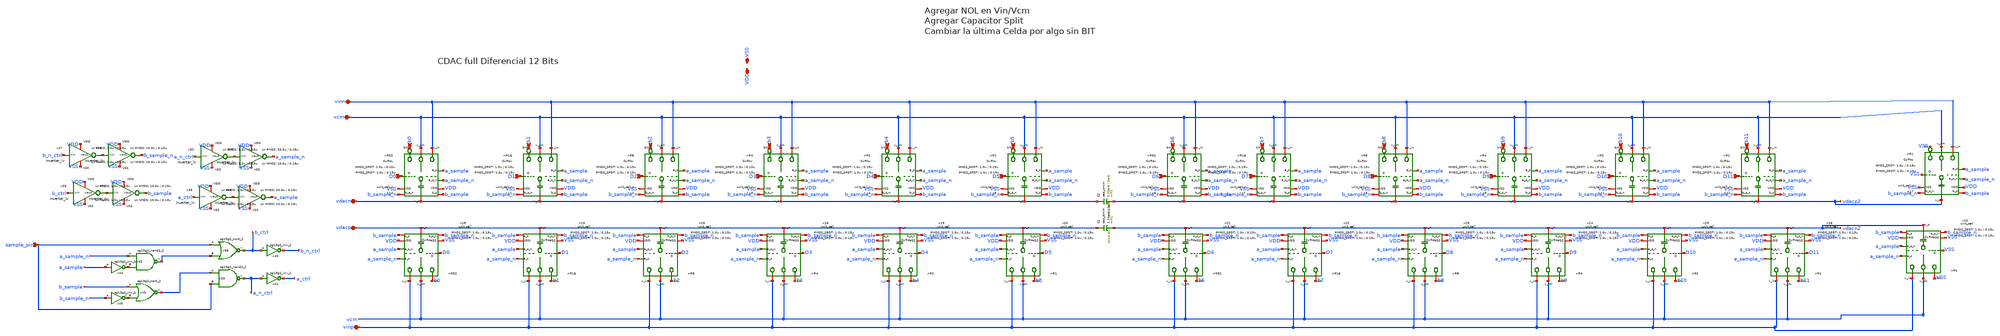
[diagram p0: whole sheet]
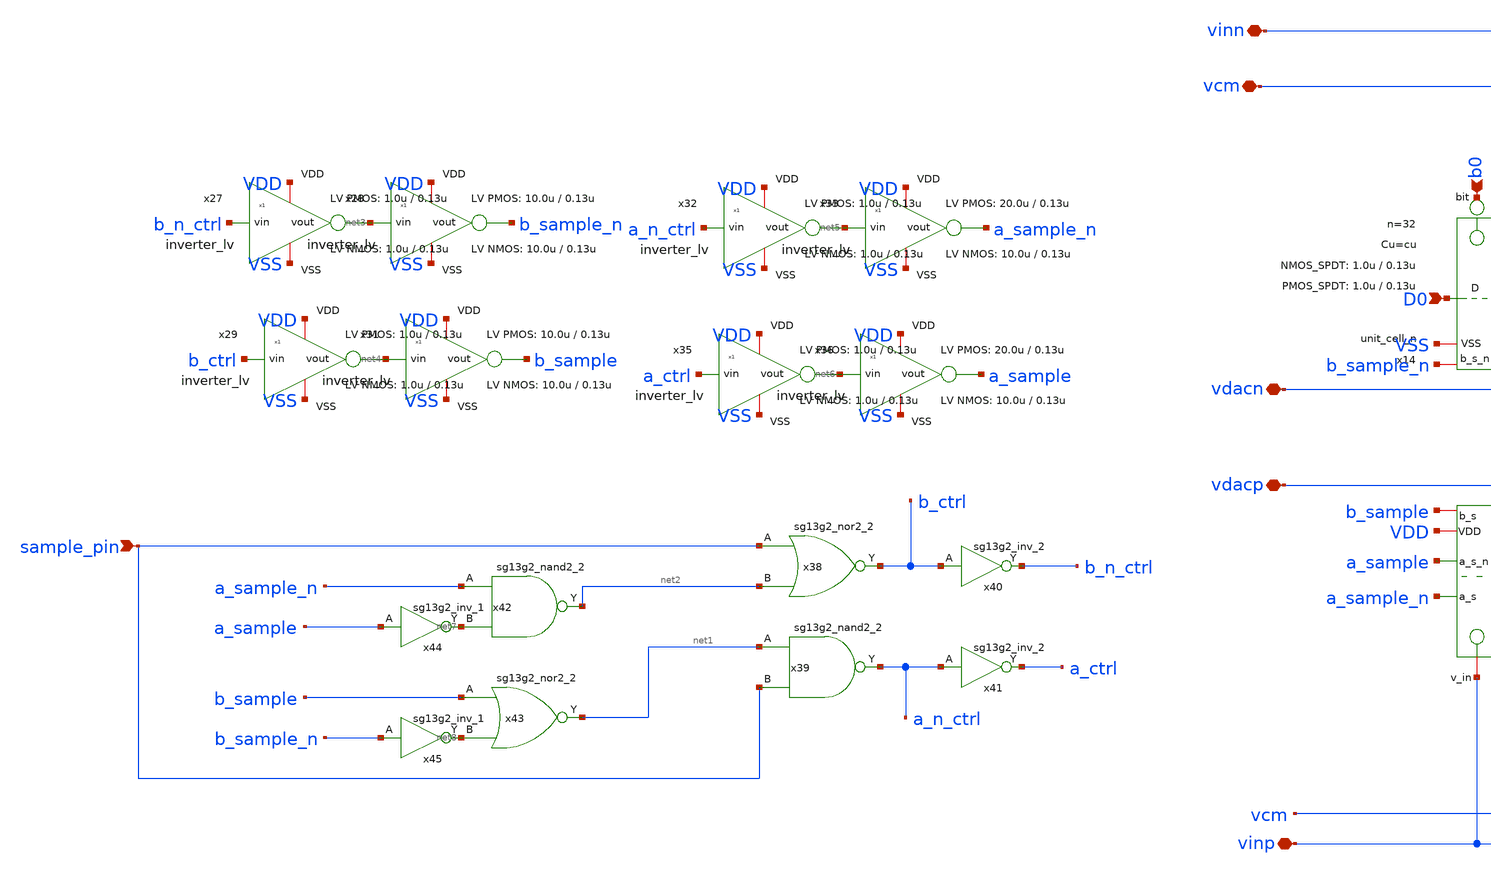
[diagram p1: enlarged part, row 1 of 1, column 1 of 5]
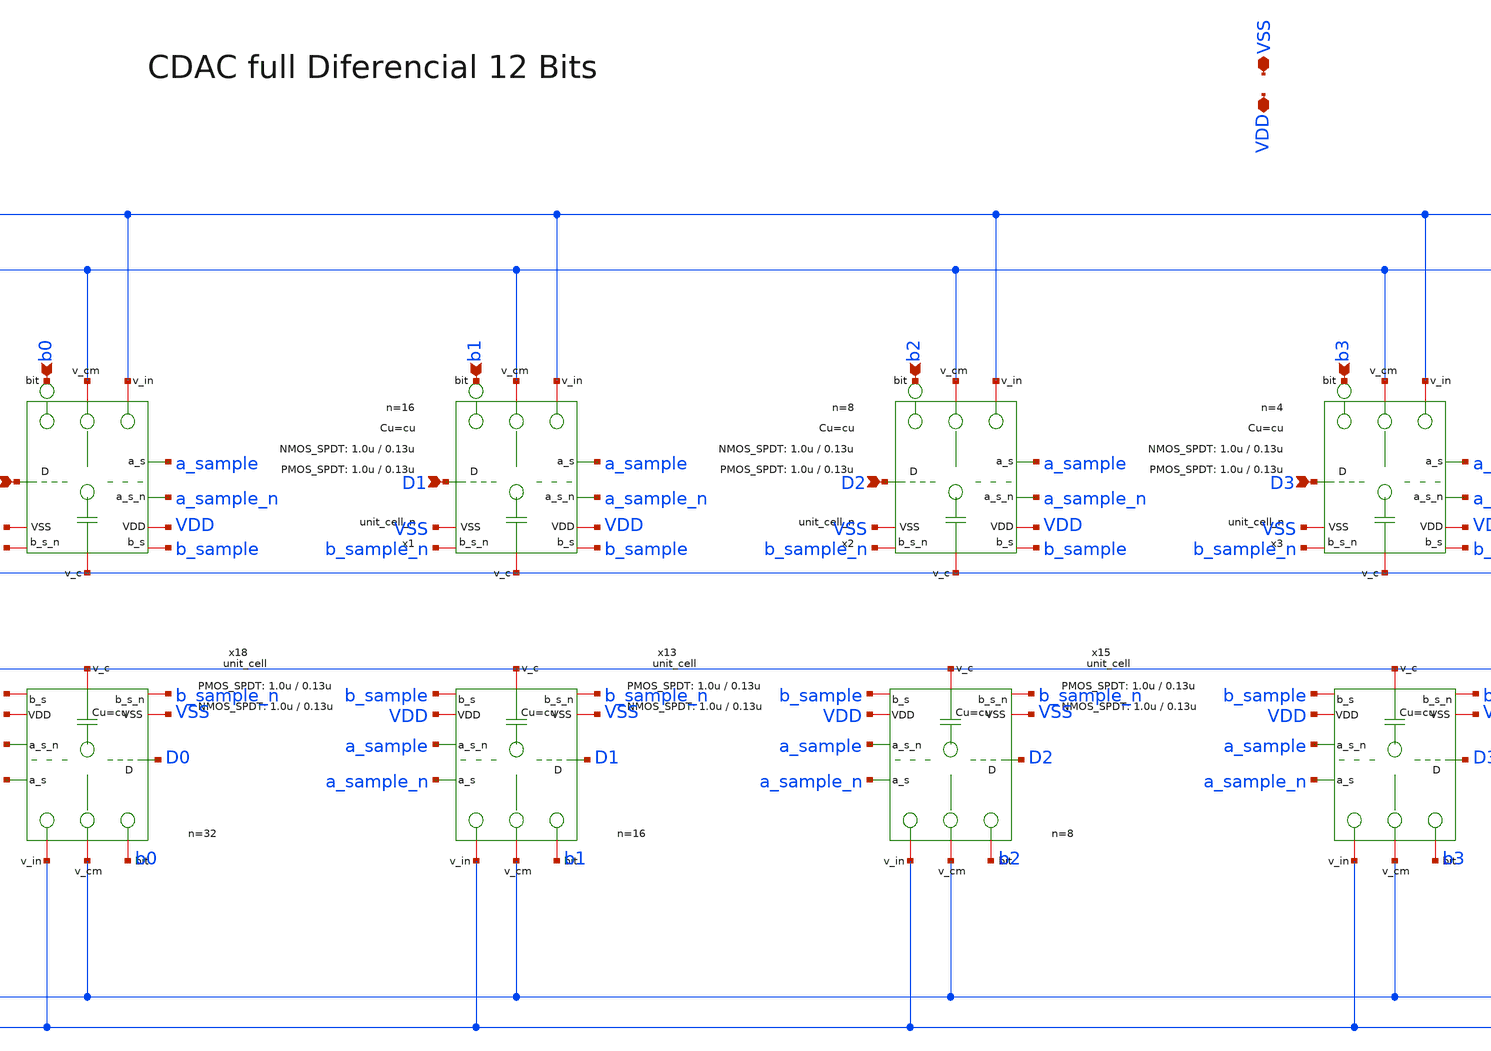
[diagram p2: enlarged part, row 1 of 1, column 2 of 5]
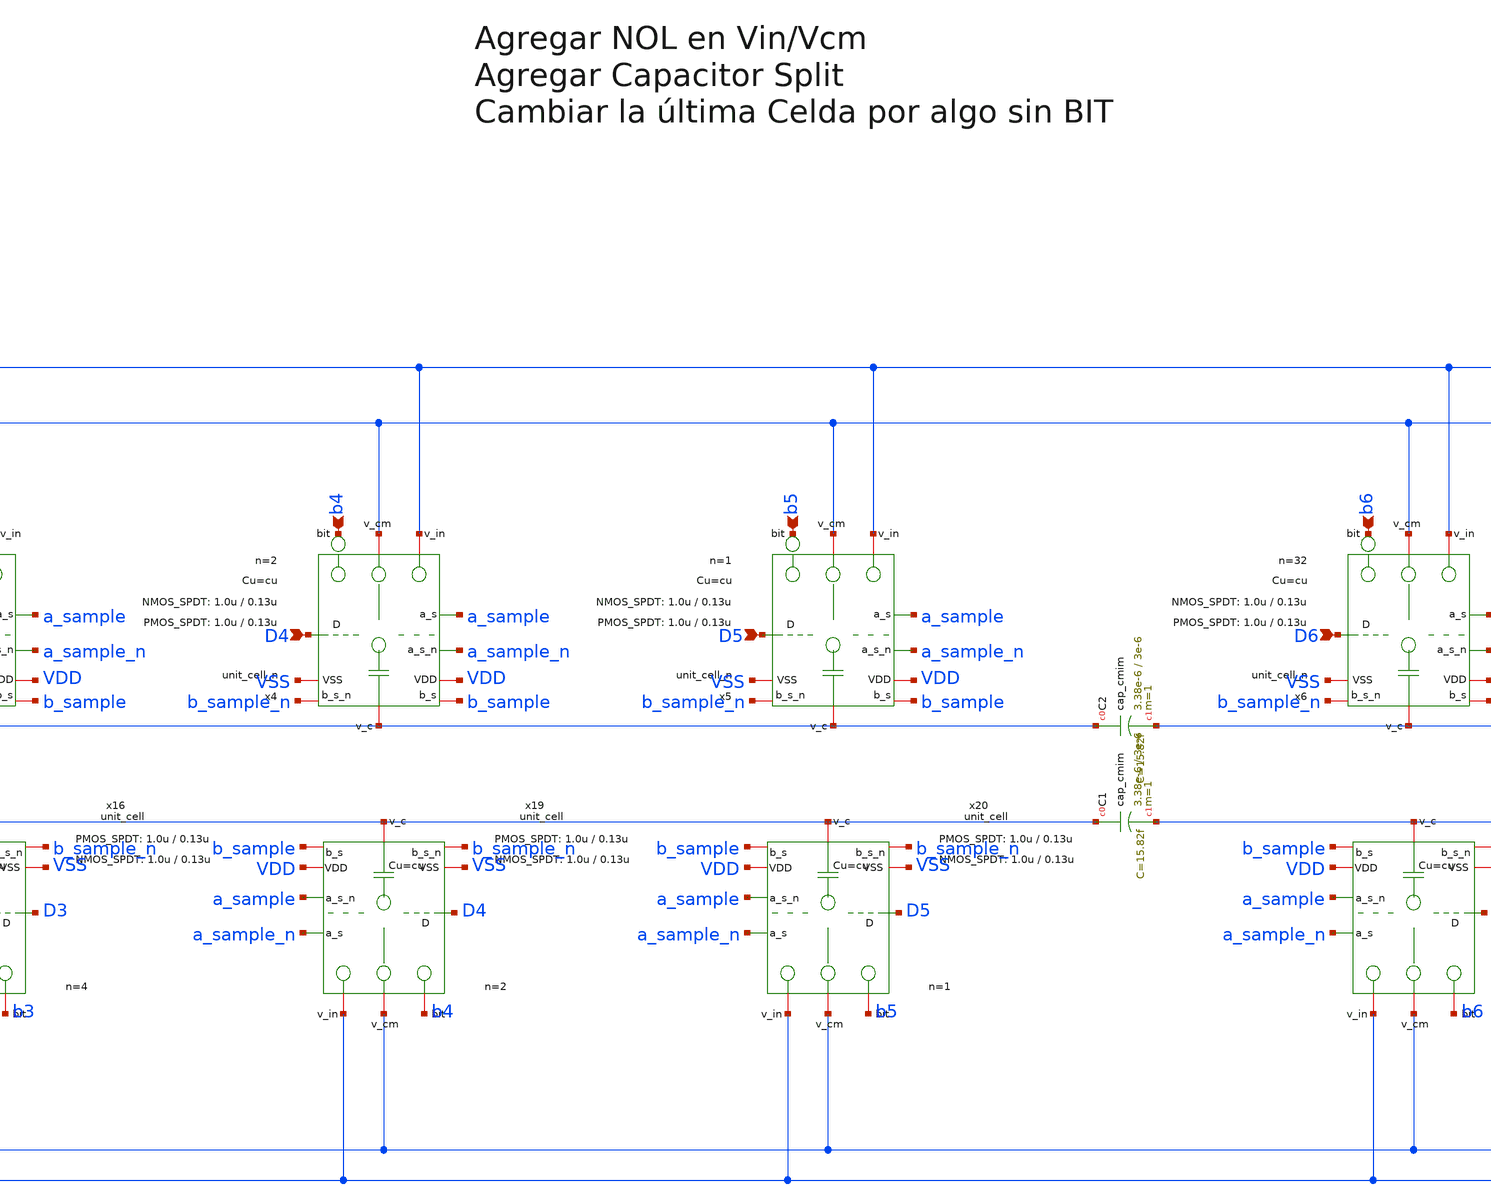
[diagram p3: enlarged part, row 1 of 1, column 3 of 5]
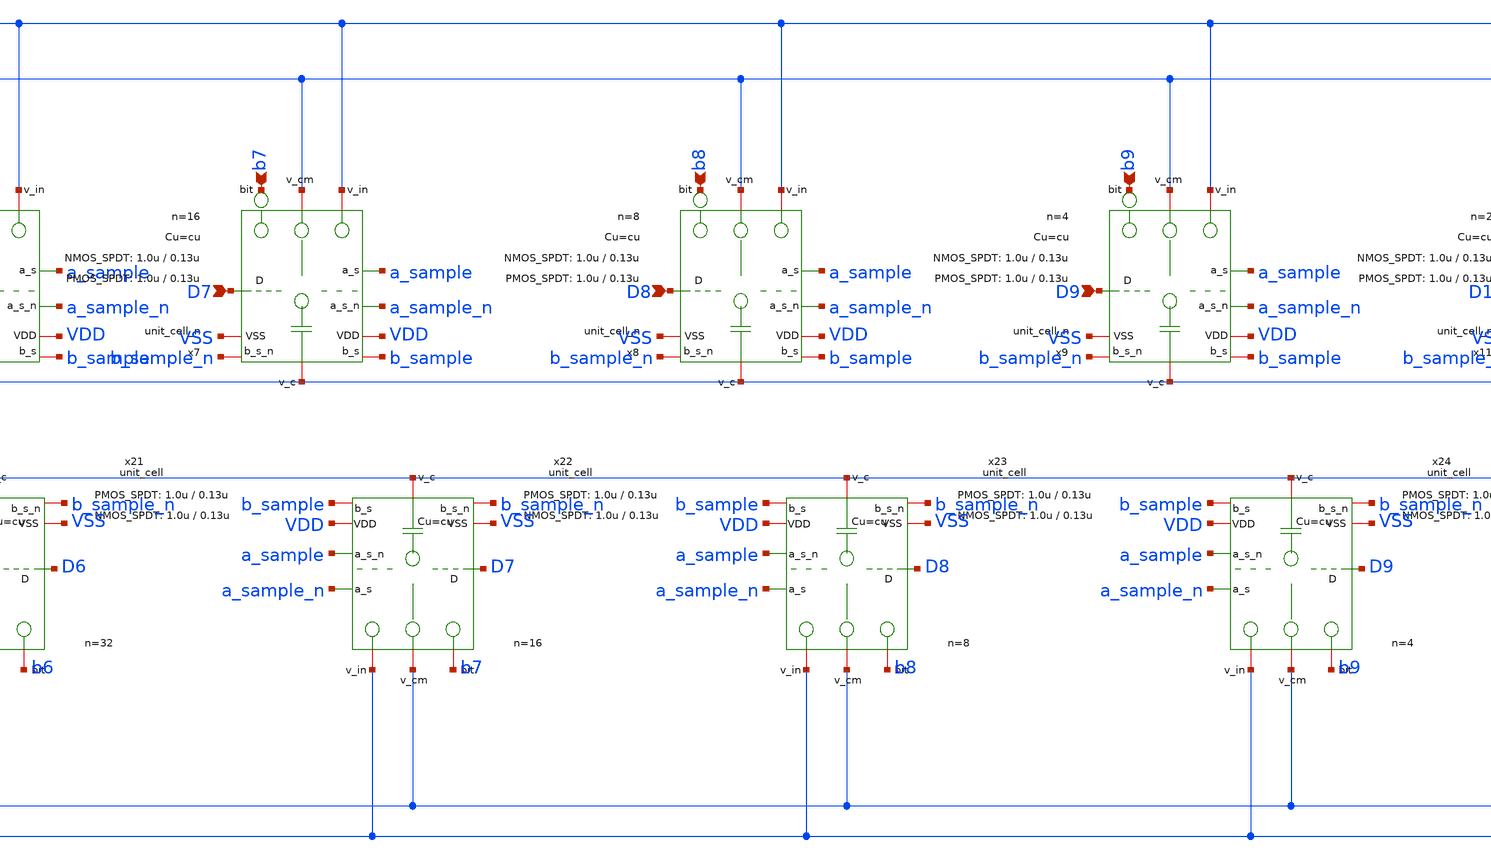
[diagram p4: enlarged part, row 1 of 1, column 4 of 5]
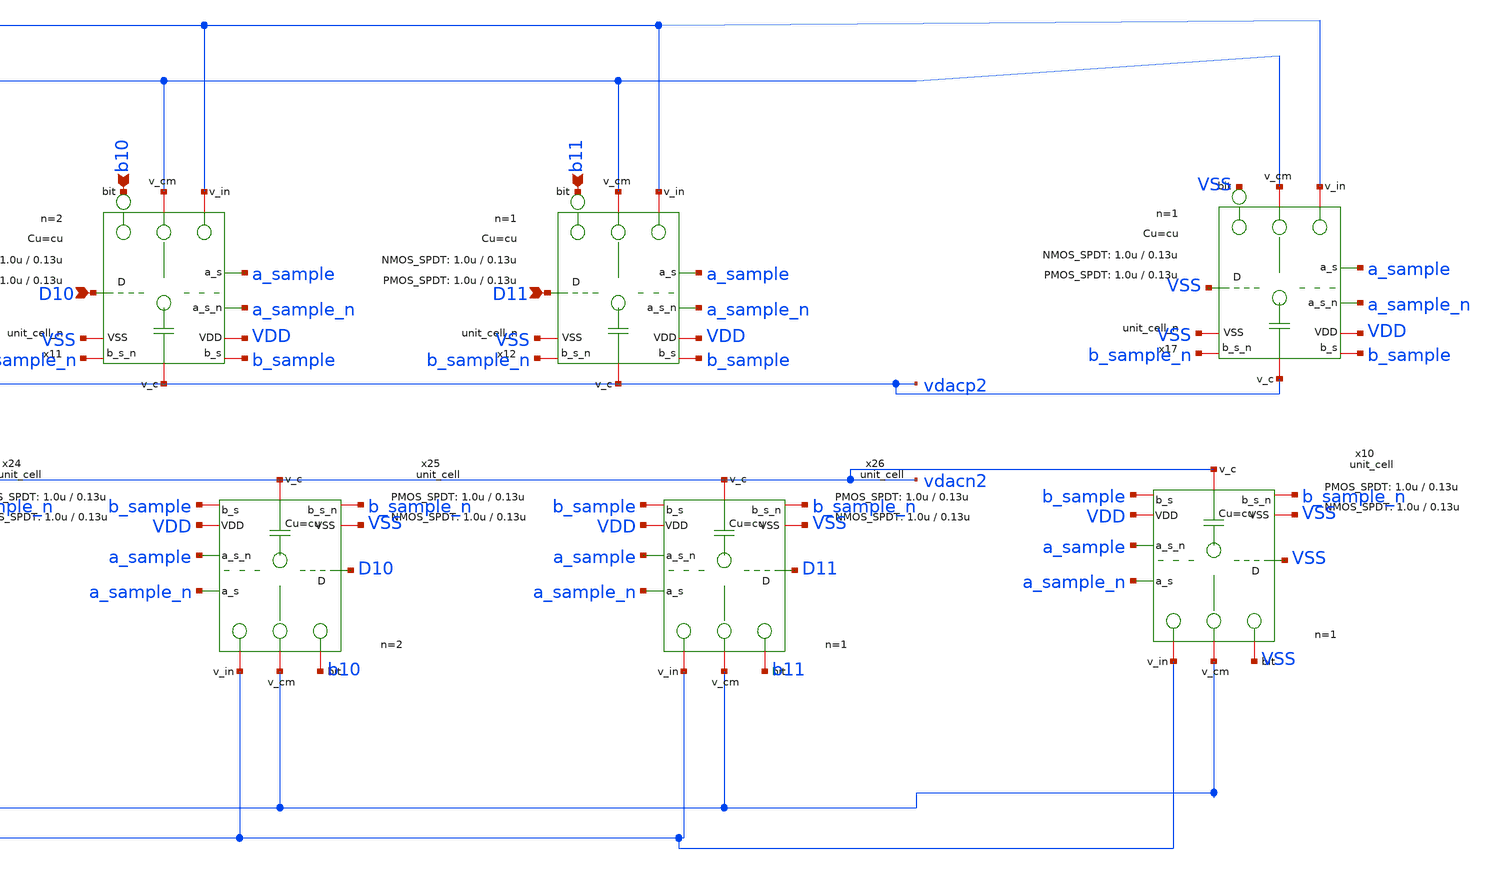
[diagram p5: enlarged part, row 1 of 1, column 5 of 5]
** sch_path: xschem/dac_icms_cell/dac.sch
* IHP-GmbH/IHP-Open-PDK/ihp-sg13g2/libs.tech/xschem/sg13g2_stdcells/sg13g2_inv_2.sch:
* Copyright 2023 IHP PDK Authors
* Licensed under the Apache License, Version 2.0 (the "License");
**.subckt dac D0 b0 vinp vcm sample_pin vinn vdacp vdacn VSS VDD D1 b1 D2 b2 D3 b3 D4 b4 D5 b5 D6 b6
*+ D7 b7 D8 b8 D9 b9 D10 b10 D11 b11
*.ipin D0
*.ipin b0
*.iopin vinp
*.iopin vcm
*.ipin sample_pin
*.iopin vinn
*.iopin vdacp
*.iopin vdacn
*.iopin VSS
*.iopin VDD
*.ipin D1
*.ipin b1
*.ipin D2
*.ipin b2
*.ipin D3
*.ipin b3
*.ipin D4
*.ipin b4
*.ipin D5
*.ipin b5
*.ipin D6
*.ipin b6
*.ipin D7
*.ipin b7
*.ipin D8
*.ipin b8
*.ipin D9
*.ipin b9
*.ipin D10
*.ipin b10
*.ipin D11
*.ipin b11
x14 VDD D0 VSS vdacn b0 vcm vinn a_sample a_sample_n b_sample b_sample_n unit_cell_n W_P=
+ L_P_SPDT=0.13u W_N= L_N_SPDT=0.13u Cu=cu n=32
x18 VDD D0 VSS vdacp b0 vcm vinp a_sample_n a_sample b_sample b_sample_n unit_cell W_P=
+ L_P_SPDT=0.13u W_N= L_N_SPDT=0.13u Cu=cu n=32
x1 VDD D1 VSS vdacn b1 vcm vinn a_sample a_sample_n b_sample b_sample_n unit_cell_n W_P=
+ L_P_SPDT=0.13u W_N= L_N_SPDT=0.13u Cu=cu n=16
x2 VDD D2 VSS vdacn b2 vcm vinn a_sample a_sample_n b_sample b_sample_n unit_cell_n W_P=
+ L_P_SPDT=0.13u W_N= L_N_SPDT=0.13u Cu=cu n=8
x3 VDD D3 VSS vdacn b3 vcm vinn a_sample a_sample_n b_sample b_sample_n unit_cell_n W_P=
+ L_P_SPDT=0.13u W_N= L_N_SPDT=0.13u Cu=cu n=4
x4 VDD D4 VSS vdacn b4 vcm vinn a_sample a_sample_n b_sample b_sample_n unit_cell_n W_P=1.0u
+ L_P_SPDT=0.13u W_N=1.0u L_N_SPDT=0.13u Cu=cu n=2
x5 VDD D5 VSS vdacn b5 vcm vinn a_sample a_sample_n b_sample b_sample_n unit_cell_n W_P=
+ L_P_SPDT=0.13u W_N= L_N_SPDT=0.13u Cu=cu n=1
x6 VDD D6 VSS vdacp2 b6 vcm vinn a_sample a_sample_n b_sample b_sample_n unit_cell_n W_P=
+ L_P_SPDT=0.13u W_N= L_N_SPDT=0.13u Cu=cu n=32
x7 VDD D7 VSS vdacp2 b7 vcm vinn a_sample a_sample_n b_sample b_sample_n unit_cell_n W_P=
+ L_P_SPDT=0.13u W_N= L_N_SPDT=0.13u Cu=cu n=16
x8 VDD D8 VSS vdacp2 b8 vcm vinn a_sample a_sample_n b_sample b_sample_n unit_cell_n W_P=
+ L_P_SPDT=0.13u W_N= L_N_SPDT=0.13u Cu=cu n=8
x9 VDD D9 VSS vdacp2 b9 vcm vinn a_sample a_sample_n b_sample b_sample_n unit_cell_n W_P=
+ L_P_SPDT=0.13u W_N= L_N_SPDT=0.13u Cu=cu n=4
x11 VDD D10 VSS vdacp2 b10 vcm vinn a_sample a_sample_n b_sample b_sample_n unit_cell_n W_P=
+ L_P_SPDT=0.13u W_N= L_N_SPDT=0.13u Cu=cu n=2
x12 VDD D11 VSS vdacp2 b11 vcm vinn a_sample a_sample_n b_sample b_sample_n unit_cell_n W_P=
+ L_P_SPDT=0.13u W_N= L_N_SPDT=0.13u Cu=cu n=1
x13 VDD D1 VSS vdacp b1 vcm vinp a_sample_n a_sample b_sample b_sample_n unit_cell W_P=
+ L_P_SPDT=0.13u W_N= L_N_SPDT=0.13u Cu=cu n=16
x15 VDD D2 VSS vdacp b2 vcm vinp a_sample_n a_sample b_sample b_sample_n unit_cell W_P=
+ L_P_SPDT=0.13u W_N= L_N_SPDT=0.13u Cu=cu n=8
x16 VDD D3 VSS vdacp b3 vcm vinp a_sample_n a_sample b_sample b_sample_n unit_cell W_P=
+ L_P_SPDT=0.13u W_N= L_N_SPDT=0.13u Cu=cu n=4
x19 VDD D4 VSS vdacp b4 vcm vinp a_sample_n a_sample b_sample b_sample_n unit_cell W_P=1.0u
+ L_P_SPDT=0.13u W_N=1.0u L_N_SPDT=0.13u Cu=cu n=2
x20 VDD D5 VSS vdacp b5 vcm vinp a_sample_n a_sample b_sample b_sample_n unit_cell W_P=
+ L_P_SPDT=0.13u W_N= L_N_SPDT=0.13u Cu=cu n=1
x21 VDD D6 VSS vdacn2 b6 vcm vinp a_sample_n a_sample b_sample b_sample_n unit_cell W_P=
+ L_P_SPDT=0.13u W_N= L_N_SPDT=0.13u Cu=cu n=32
x22 VDD D7 VSS vdacn2 b7 vcm vinp a_sample_n a_sample b_sample b_sample_n unit_cell W_P=
+ L_P_SPDT=0.13u W_N= L_N_SPDT=0.13u Cu=cu n=16
x23 VDD D8 VSS vdacn2 b8 vcm vinp a_sample_n a_sample b_sample b_sample_n unit_cell W_P=
+ L_P_SPDT=0.13u W_N= L_N_SPDT=0.13u Cu=cu n=8
x24 VDD D9 VSS vdacn2 b9 vcm vinp a_sample_n a_sample b_sample b_sample_n unit_cell W_P=
+ L_P_SPDT=0.13u W_N= L_N_SPDT=0.13u Cu=cu n=4
x25 VDD D10 VSS vdacn2 b10 vcm vinp a_sample_n a_sample b_sample b_sample_n unit_cell W_P=
+ L_P_SPDT=0.13u W_N= L_N_SPDT=0.13u Cu=cu n=2
x26 VDD D11 VSS vdacn2 b11 vcm vinp a_sample_n a_sample b_sample b_sample_n unit_cell W_P=
+ L_P_SPDT=0.13u W_N= L_N_SPDT=0.13u Cu=cu n=1
x27 VDD b_n_ctrl net3 VSS inverter_lv W_P=1.0u L_P=0.13u W_N=1.0u L_N=0.13u N_C=1
x28 VDD net3 b_sample_n VSS inverter_lv W_P=10.0u L_P=0.13u W_N=10.0u L_N=0.13u N_C=1
x29 VDD b_ctrl net4 VSS inverter_lv W_P=1.0u L_P=0.13u W_N=1.0u L_N=0.13u N_C=1
x31 VDD net4 b_sample VSS inverter_lv W_P=10.0u L_P=0.13u W_N=10.0u L_N=0.13u N_C=1
x32 VDD a_n_ctrl net5 VSS inverter_lv W_P=1.0u L_P=0.13u W_N=1.0u L_N=0.13u N_C=1
x33 VDD net5 a_sample_n VSS inverter_lv W_P=20.0u L_P=0.13u W_N=10.0u L_N=0.13u N_C=1
x35 VDD a_ctrl net6 VSS inverter_lv W_P=1.0u L_P=0.13u W_N=1.0u L_N=0.13u N_C=1
x36 VDD net6 a_sample VSS inverter_lv W_P=20.0u L_P=0.13u W_N=10.0u L_N=0.13u N_C=1
x38 b_ctrl sample_pin net2 VDD VSS sg13g2_nor2_2
x39 a_n_ctrl net1 sample_pin VDD VSS sg13g2_nand2_2
x40 b_n_ctrl b_ctrl VDD VSS sg13g2_inv_2
x41 a_ctrl a_n_ctrl VDD VSS sg13g2_inv_2
x42 net2 a_sample_n net7 VDD VSS sg13g2_nand2_2
x43 net1 b_sample net8 VDD VSS sg13g2_nor2_2
x44 net7 a_sample VDD VSS sg13g2_inv_1
x45 net8 b_sample_n VDD VSS sg13g2_inv_1
XC1 vdacp vdacn2 cap_cmim w=3.38e-6 l=3e-6 m=1 mm_ok=1
XC2 vdacn vdacp2 cap_cmim w=3.38e-6 l=3e-6 m=1 mm_ok=1
x10 VDD VSS VSS vdacn2 VSS vcm vinp a_sample_n a_sample b_sample b_sample_n unit_cell W_P=
+ L_P_SPDT=0.13u W_N= L_N_SPDT=0.13u Cu=cu n=1
x17 VDD VSS VSS vdacp2 VSS vcm vinn a_sample a_sample_n b_sample b_sample_n unit_cell_n W_P=
+ L_P_SPDT=0.13u W_N= L_N_SPDT=0.13u Cu=cu n=1
**.ends

* expanding   symbol:  dac_icms_cell/unit_cell_n.sym # of pins=11
** sym_path: xschem/dac_icms_cell/unit_cell_n.sym
** sch_path: xschem/dac_icms_cell/unit_cell_n.sch
.subckt unit_cell_n VDD d VSS v_top bit v_cm v_in a_sample a_sample_n b_sample b_sample_n
+  W_P_SPDT=1.0u L_P_SPDT=0.13u W_N_SPDT=1.0u L_N_SPDT=0.13u Cu=8f n=1
*.iopin VSS
*.iopin v_in
*.iopin VDD
*.ipin d
*.ipin bit
*.iopin v_top
*.iopin v_cm
*.ipin a_sample
*.ipin a_sample_n
*.ipin b_sample
*.ipin b_sample_n
x1 VDD d VSS net1 bit v_cm v_in b_sample_n b_sample dac_switch_n W_P=W_P L_P_TG=0.13u W_N=W_N
+ L_N_TG=0.13u n=n
x2 VDD a_sample VSS v_top v_cm a_sample_n transmission_gate_lv_wo_dummy W_P=W_P_SPDT L_P=L_P_SPDT
+ W_N=W_N_SPDT L_N=L_N_SPDT W_P_D=1.0u L_P_D=0.13u W_N_D=1.0u L_N_D=0.13u n=n
XC1 net1 v_top cap_cmim w=3e-6 l=3e-6 m=n mm_ok=1
.ends


* expanding   symbol:  dac_icms_cell/unit_cell.sym # of pins=11
** sym_path: xschem/dac_icms_cell/unit_cell.sym
** sch_path: xschem/dac_icms_cell/unit_cell.sch
.subckt unit_cell VDD d VSS v_top bit v_cm v_in a_sample a_sample_n b_sample b_sample_n
+  W_P_SPDT=1.0u L_P_SPDT=0.13u W_N_SPDT=1.0u L_N_SPDT=0.13u Cu=8f n=1
*.iopin VSS
*.iopin v_in
*.iopin VDD
*.ipin d
*.ipin bit
*.iopin v_top
*.iopin v_cm
*.ipin a_sample_n
*.ipin a_sample
*.ipin b_sample
*.ipin b_sample_n
x1 VDD d VSS net1 bit v_cm v_in b_sample_n b_sample dac_switch W_P=W_P L_P_TG=0.13u W_N=W_N
+ L_N_TG=0.13u n=n
x2 VDD a_sample_n VSS v_top v_cm a_sample transmission_gate_lv_wo_dummy W_P=W_P_SPDT L_P=L_P_SPDT
+ W_N=W_N_SPDT L_N=L_N_SPDT W_P_D=1.0u L_P_D=0.13u W_N_D=1.0u L_N_D=0.13u n=n
XC1 net1 v_top cap_cmim w=3e-6 l=3e-6 m=n mm_ok=1
.ends


* expanding   symbol:  inverter/inverter_lv.sym # of pins=4
** sym_path: xschem/inverter/inverter_lv.sym
** sch_path: xschem/inverter/inverter_lv.sch
.subckt inverter_lv VDD vin vout VSS  W_P=3.0u L_P=0.13u W_N=1.0u L_N=0.13u N_C=1
*.ipin vin
*.iopin VDD
*.iopin VSS
*.opin vout
XM1 vout vin VDD VDD sg13_lv_pmos w=W_P l=L_P ng=1 m={N_C} mm_ok=1
XM2 vout vin VSS VSS sg13_lv_nmos w=W_N l=L_N ng=1 m={N_C} mm_ok=1
.ends


* expanding   symbol:  sg13g2_stdcells/sg13g2_nor2_2.sym # of pins=3
** sym_path: sg13g2_stdcells/sg13g2_nor2_2.sym
** sch_path: sg13g2_stdcells/sg13g2_nor2_2.sch
.subckt sg13g2_nor2_2 Y A B VDD VSS
*.opin Y
*.ipin B
*.ipin A
*.iopin VDD
*.iopin VSS
XM1 Y A VSS VSS sg13_lv_nmos w=1.48u l=130.00n ng=2 m=1 mm_ok=1
XM2 Y B VSS VSS sg13_lv_nmos w=1.48u l=130.00n ng=2 m=1 mm_ok=1
XM3 net1 A VDD VDD sg13_lv_pmos w=2.24u l=130.00n ng=2 m=1 mm_ok=1
XM4 Y B net1 VDD sg13_lv_pmos w=2.24u l=130.00n ng=2 m=1 mm_ok=1
.ends


* expanding   symbol:  sg13g2_stdcells/sg13g2_nand2_2.sym # of pins=3
** sym_path: sg13g2_stdcells/sg13g2_nand2_2.sym
** sch_path: sg13g2_stdcells/sg13g2_nand2_2.sch
.subckt sg13g2_nand2_2 Y A B VDD VSS
*.iopin VDD
*.iopin VSS
*.opin Y
*.ipin B
*.ipin A
XM1 Y A net1 VSS sg13_lv_nmos w=1.44u l=130.00n ng=2 m=1 mm_ok=1
XM2 net1 B VSS VSS sg13_lv_nmos w=1.44u l=130.00n ng=2 m=1 mm_ok=1
XM3 Y A VDD VDD sg13_lv_pmos w=2.24u l=130.00n ng=2 m=1 mm_ok=1
XM4 Y B VDD VDD sg13_lv_pmos w=2.24u l=130.00n ng=2 m=1 mm_ok=1
.ends


* expanding   symbol:  sg13g2_stdcells/sg13g2_inv_2.sym # of pins=2
** sym_path: sg13g2_stdcells/sg13g2_inv_2.sym
** sch_path: sg13g2_stdcells/sg13g2_inv_2.sch
.subckt sg13g2_inv_2 Y A VDD VSS
*.opin Y
*.ipin A
*.iopin VDD
*.iopin VSS
XM1 Y A VSS VSS sg13_lv_nmos w=1.48u l=130.00n ng=2 m=1 mm_ok=1
XM2 Y A VDD VDD sg13_lv_pmos w=2.24u l=130.00n ng=2 m=1 mm_ok=1
.ends


* expanding   symbol:  sg13g2_stdcells/sg13g2_inv_1.sym # of pins=2
** sym_path: sg13g2_stdcells/sg13g2_inv_1.sym
** sch_path: sg13g2_stdcells/sg13g2_inv_1.sch
.subckt sg13g2_inv_1 Y A VDD VSS
*.opin Y
*.ipin A
*.iopin VDD
*.iopin VSS
XM1 Y A VSS VSS sg13_lv_nmos w=740.00n l=130.00n ng=1 m=1 mm_ok=1
XM2 Y A VDD VDD sg13_lv_pmos w=1.12u l=130.00n ng=1 m=1 mm_ok=1
.ends


* expanding   symbol:  dac_icms_cell/dac_switch_n.sym # of pins=9
** sym_path: xschem/dac_icms_cell/dac_switch_n.sym
** sch_path: xschem/dac_icms_cell/dac_switch_n.sch
.subckt dac_switch_n VDD d VSS v_cap bit v_cm v_in sample sample_n  W_P_TG=3.0u L_P_TG=0.13u
+ W_N_TG=1.0u L_N_TG=0.13u n=1
*.iopin v_in
*.iopin v_cap
*.iopin VDD
*.iopin VSS
*.ipin d
*.iopin v_cm
*.ipin bit
*.ipin sample
*.ipin sample_n
x8 VDD d d_n VSS inverter_lv W_P=W_P L_P=L_P_TG W_N=W_N L_N=L_N_TG N_C=1
XM1 v_cap net3 VSS VSS sg13_lv_nmos w=1u l=0.13u ng=1 m=n mm_ok=1
XM3 v_cap net4 VDD VDD sg13_lv_pmos w=1u l=0.13u ng=1 m=n mm_ok=1
x2 VDD net2 VSS v_cap v_cm net1 transmission_gate_lv_wo_dummy W_P=W_P L_P=L_P_TG W_N=W_N L_N=L_N_TG
+ W_P_D=1.0u L_P_D=0.13u W_N_D=1.0u L_N_D=0.13u n=n
x1 VDD sample VSS v_cap v_in sample_n transmission_gate_lv_w_dummy W_P=W_P L_P=L_P_TG W_N=W_N
+ L_N=L_N_TG W_P_D=1.0u L_P_D=0.13u W_N_D=1.0u L_N_D=0.13u n=n
x23 net5 bit d VDD VSS sg13g2_nand2_1
x46 net6 net9 d VDD VSS sg13g2_and2_1
x4 VDD net5 net4 VSS buffer_lv W_P_INV=3.0u L_P_INV=0.13u W_N_INV=1.0u L_N_INV=0.13u
x5 VDD net6 net3 VSS buffer_lv W_P_INV=3.0u L_P_INV=0.13u W_N_INV=1.0u L_N_INV=0.13u
x3 net7 d sample VDD VSS sg13g2_nor2_1
x6 net8 d sample VDD VSS sg13g2_or2_1
x7 VDD net7 net2 VSS buffer_lv W_P_INV=3.0u L_P_INV=0.13u W_N_INV=1.0u L_N_INV=0.13u
x9 VDD net8 net1 VSS buffer_lv W_P_INV=3.0u L_P_INV=0.13u W_N_INV=1.0u L_N_INV=0.13u
x32 net9 bit VDD VSS sg13g2_inv_1
.ends


* expanding   symbol:  transmission_gate/transmission_gate_lv_wo_dummy.sym # of pins=6
** sym_path: xschem/transmission_gate/transmission_gate_lv_wo_dummy.sym
** sch_path: xschem/transmission_gate/transmission_gate_lv_wo_dummy.sch
.subckt transmission_gate_lv_wo_dummy VDD di_tg_ctrl VSS v_b v_a di_tg_ctrl_n  W_P=2.0u L_P=0.13u
+ W_N=2.0u L_N=0.13u W_P_D=1.0u L_P_D=0.13u W_N_D=1.0u L_N_D=0.13u n=1
*.iopin v_a
*.iopin v_b
*.iopin VDD
*.iopin VSS
*.ipin di_tg_ctrl
*.ipin di_tg_ctrl_n
XM1 v_a di_tg_ctrl v_b VSS sg13_lv_nmos w=W_N l=L_N ng=1 m=n mm_ok=1
XM2 v_a di_tg_ctrl_n v_b VDD sg13_lv_pmos w=W_P l=L_P ng=1 m=n mm_ok=1
.ends


* expanding   symbol:  dac_icms_cell/dac_switch.sym # of pins=9
** sym_path: xschem/dac_icms_cell/dac_switch.sym
** sch_path: xschem/dac_icms_cell/dac_switch.sch
.subckt dac_switch VDD d VSS v_cap bit v_cm v_in sample sample_n  W_P_TG=3.0u L_P_TG=0.13u
+ W_N_TG=1.0u L_N_TG=0.13u n=1
*.iopin v_in
*.iopin v_cap
*.iopin VDD
*.iopin VSS
*.ipin d
*.ipin bit
*.ipin sample
*.ipin sample_n
*.iopin v_cm
x8 VDD d d_n VSS inverter_lv W_P=W_P L_P=L_P_TG W_N=W_N L_N=L_N_TG N_C=1
XM1 v_cap net1 VSS VSS sg13_lv_nmos w=1u l=0.13u ng=1 m=n mm_ok=1
XM3 v_cap net2 VDD VDD sg13_lv_pmos w=1u l=0.13u ng=1 m=n mm_ok=1
x1 VDD sample VSS v_cap v_in sample_n transmission_gate_lv_w_dummy W_P=W_P L_P=L_P_TG W_N=W_N
+ L_N=L_N_TG W_P_D=1.0u L_P_D=0.13u W_N_D=1.0u L_N_D=0.13u n=n
x23 net3 net9 d VDD VSS sg13g2_nand2_1
x46 net4 bit d VDD VSS sg13g2_and2_1
x4 VDD net3 net2 VSS buffer_lv W_P_INV=3.0u L_P_INV=0.13u W_N_INV=1.0u L_N_INV=0.13u
x5 VDD net4 net1 VSS buffer_lv W_P_INV=3.0u L_P_INV=0.13u W_N_INV=1.0u L_N_INV=0.13u
x32 net9 bit VDD VSS sg13g2_inv_1
x3 VDD net6 VSS v_cap v_cm net5 transmission_gate_lv_wo_dummy W_P=W_P L_P=L_P_TG W_N=W_N L_N=L_N_TG
+ W_P_D=1.0u L_P_D=0.13u W_N_D=1.0u L_N_D=0.13u n=n
x6 net7 d sample VDD VSS sg13g2_nor2_1
x7 net8 d sample VDD VSS sg13g2_or2_1
x9 VDD net7 net6 VSS buffer_lv W_P_INV=3.0u L_P_INV=0.13u W_N_INV=1.0u L_N_INV=0.13u
x10 VDD net8 net5 VSS buffer_lv W_P_INV=3.0u L_P_INV=0.13u W_N_INV=1.0u L_N_INV=0.13u
.ends


* expanding   symbol:  transmission_gate/transmission_gate_lv_w_dummy.sym # of pins=6
** sym_path: xschem/transmission_gate/transmission_gate_lv_w_dummy.sym
** sch_path: xschem/transmission_gate/transmission_gate_lv_w_dummy.sch
.subckt transmission_gate_lv_w_dummy VDD di_tg_ctrl VSS v_b v_a di_tg_ctrl_n  W_P=2.0u L_P=0.13u
+ W_N=2.0u L_N=0.13u W_P_D=1.0u L_P_D=0.13u W_N_D=1.0u L_N_D=0.13u n=1
*.iopin v_a
*.iopin v_b
*.iopin VDD
*.iopin VSS
*.ipin di_tg_ctrl
*.ipin di_tg_ctrl_n
XM1 v_a di_tg_ctrl v_b VSS sg13_lv_nmos w=W_N l=L_N ng=1 m={2*n} mm_ok=1
XM2 v_a di_tg_ctrl_n v_b VDD sg13_lv_pmos w=W_P l=L_P ng=1 m={2*n} mm_ok=1
XMdummy2 v_b di_tg_ctrl v_b VDD sg13_lv_pmos w=W_P l=L_P ng=1 m=n mm_ok=1
XMdummy1 v_b di_tg_ctrl_n v_b VSS sg13_lv_nmos w=W_N l=L_N ng=1 m=n mm_ok=1
.ends


* expanding   symbol:  sg13g2_stdcells/sg13g2_nand2_1.sym # of pins=3
** sym_path: sg13g2_stdcells/sg13g2_nand2_1.sym
** sch_path: sg13g2_stdcells/sg13g2_nand2_1.sch
.subckt sg13g2_nand2_1 Y A B VDD VSS
*.iopin VDD
*.iopin VSS
*.ipin A
*.ipin B
*.opin Y
XM1 Y A net1 VSS sg13_lv_nmos w=740.00n l=130.00n ng=1 m=1 mm_ok=1
XM2 net1 B VSS VSS sg13_lv_nmos w=740.00n l=130.00n ng=1 m=1 mm_ok=1
XM3 Y A VDD VDD sg13_lv_pmos w=1.12u l=130.00n ng=1 m=1 mm_ok=1
XM4 Y B VDD VDD sg13_lv_pmos w=1.12u l=130.00n ng=1 m=1 mm_ok=1
.ends


* expanding   symbol:  sg13g2_stdcells/sg13g2_and2_1.sym # of pins=3
** sym_path: sg13g2_stdcells/sg13g2_and2_1.sym
** sch_path: sg13g2_stdcells/sg13g2_and2_1.sch
.subckt sg13g2_and2_1 X A B VDD VSS
*.ipin A
*.ipin B
*.opin X
*.iopin VDD
*.iopin VSS
XM1 net1 A net2 VSS sg13_lv_nmos w=640.00n l=130.00n ng=1 m=1 mm_ok=1
XM2 net2 B VSS VSS sg13_lv_nmos w=640.00n l=130.00n ng=1 m=1 mm_ok=1
XM3 X net1 VSS VSS sg13_lv_nmos w=740.00n l=130.00n ng=1 m=1 mm_ok=1
XM4 net1 B VDD VDD sg13_lv_pmos w=840.00n l=130.00n ng=1 m=1 mm_ok=1
XM5 net1 A VDD VDD sg13_lv_pmos w=840.00n l=130.00n ng=1 m=1 mm_ok=1
XM6 X net1 VDD VDD sg13_lv_pmos w=1.12u l=130.00n ng=1 m=1 mm_ok=1
.ends


* expanding   symbol:  buffer/buffer_lv.sym # of pins=4
** sym_path: buffer/buffer_lv.sym
** sch_path: buffer/buffer_lv.sch
.subckt buffer_lv VDD vin vout VSS  W_P_INV=3.0u L_P_INV=0.13u W_N_INV=1.0u L_N_INV=0.13u
*.ipin vin
*.iopin VDD
*.iopin VSS
*.opin vout
x1 VDD vin net1 VSS inverter_lv W_P=W_P_INV L_P=L_P_INV W_N=W_N_INV L_N=L_N_INV N_C=1
x2 VDD net1 vout VSS inverter_lv W_P=W_P_INV L_P=L_P_INV W_N=W_N_INV L_N=L_N_INV N_C=1
.ends


* expanding   symbol:  sg13g2_stdcells/sg13g2_nor2_1.sym # of pins=3
** sym_path: sg13g2_stdcells/sg13g2_nor2_1.sym
** sch_path: sg13g2_stdcells/sg13g2_nor2_1.sch
.subckt sg13g2_nor2_1 Y A B VDD VSS
*.opin Y
*.ipin B
*.ipin A
*.iopin VDD
*.iopin VSS
XM1 Y A VSS VSS sg13_lv_nmos w=740.00n l=130.00n ng=1 m=1 mm_ok=1
XM2 Y B VSS VSS sg13_lv_nmos w=740.00n l=130.00n ng=1 m=1 mm_ok=1
XM3 net1 A VDD VDD sg13_lv_pmos w=1.12u l=130.00n ng=1 m=1 mm_ok=1
XM4 Y B net1 VDD sg13_lv_pmos w=1.12u l=130.00n ng=1 m=1 mm_ok=1
.ends


* expanding   symbol:  sg13g2_stdcells/sg13g2_or2_1.sym # of pins=3
** sym_path: sg13g2_stdcells/sg13g2_or2_1.sym
** sch_path: sg13g2_stdcells/sg13g2_or2_1.sch
.subckt sg13g2_or2_1 X A B VDD VSS
*.opin X
*.ipin B
*.ipin A
*.iopin VDD
*.iopin VSS
XM1 net1 B VSS VSS sg13_lv_nmos w=550.00n l=130.00n ng=1 m=1 mm_ok=1
XM2 net1 A VSS VSS sg13_lv_nmos w=550.00n l=130.00n ng=1 m=1 mm_ok=1
XM3 X net1 VSS VSS sg13_lv_nmos w=740.00n l=130.00n ng=1 m=1 mm_ok=1
XM4 net2 A VDD VDD sg13_lv_pmos w=840.00n l=130.00n ng=1 m=1 mm_ok=1
XM5 net1 B net2 VDD sg13_lv_pmos w=840.00n l=130.00n ng=1 m=1 mm_ok=1
XM6 X net1 VDD VDD sg13_lv_pmos w=1.12u l=130.00n ng=1 m=1 mm_ok=1
.ends

.end
